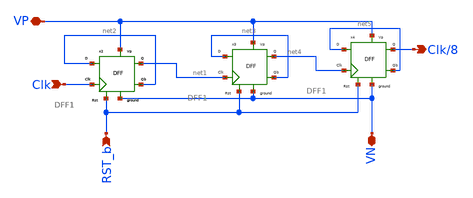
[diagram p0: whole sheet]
** sch_path: Blocks/Divide by 8 ckt/div8.sch
**.subckt div8 Clk Clk/8 RST_b VN VP
*.ipin Clk
*.opin Clk/8
*.ipin RST_b
*.iopin VN
*.iopin VP
x1 net2 Clk RST_b VN VP net1 net2 DFF1
x2 net2 Clk RST_b VN VP net1 net2 DFF1
x3 net3 net1 RST_b VN VP net4 net3 DFF1
x4 net5 net4 RST_b VN VP Clk/8 net5 DFF1
**.ends

* expanding   symbol:  PICO_2022/FlipFlops/DFF1.sym # of pins=7
** sym_path: component/FlipFlops/DFF1.sym
** sch_path: component/FlipFlops/DFF1.sch
.subckt DFF1 D Clk RST VN VP Q Qb
*.opin Q
*.iopin VN
*.iopin VP
*.ipin Clk
*.ipin D
*.ipin RST
*.opin Qb
x7 net2 net4 net3 VP VN NAND
x8 net3 Clk RST VP VN net2 NAND3
x6 Q net1 RST VP VN Qb NAND3
x4 net2 Clk net4 VP VN net1 NAND3
x5 net1 D RST VP VN net4 NAND3
x1 Qb net2 Q VP VN NAND
.ends


* expanding   symbol:  component/NAND2/NAND.sym # of pins=5
** sym_path: component/NAND2/NAND.sym
** sch_path: component/NAND2/NAND.sch
.subckt NAND B A Y VP VN
*.iopin VP
*.ipin A
*.ipin B
*.opin Y
*.iopin VN
XM1 Y A VP VP sky130_fd_pr__pfet_01v8 L=0.15 W=1.26 nf=1 ad='int((nf+1)/2) * W/nf * 0.29' as='int((nf+2)/2) * W/nf * 0.29'
+ pd='2*int((nf+1)/2) * (W/nf + 0.29)' ps='2*int((nf+2)/2) * (W/nf + 0.29)' nrd='0.29 / W' nrs='0.29 / W'
+ sa=0 sb=0 sd=0 mult=1 m=1
XM2 Y B VP VP sky130_fd_pr__pfet_01v8 L=0.15 W=1.26 nf=1 ad='int((nf+1)/2) * W/nf * 0.29' as='int((nf+2)/2) * W/nf * 0.29'
+ pd='2*int((nf+1)/2) * (W/nf + 0.29)' ps='2*int((nf+2)/2) * (W/nf + 0.29)' nrd='0.29 / W' nrs='0.29 / W'
+ sa=0 sb=0 sd=0 mult=1 m=1
XM3 Y A net1 net1 sky130_fd_pr__nfet_01v8 L=0.15 W=0.84 nf=1 ad='int((nf+1)/2) * W/nf * 0.29' as='int((nf+2)/2) * W/nf * 0.29'
+ pd='2*int((nf+1)/2) * (W/nf + 0.29)' ps='2*int((nf+2)/2) * (W/nf + 0.29)' nrd='0.29 / W' nrs='0.29 / W'
+ sa=0 sb=0 sd=0 mult=1 m=1
XM4 net1 B VN VN sky130_fd_pr__nfet_01v8 L=0.15 W=0.84 nf=1 ad='int((nf+1)/2) * W/nf * 0.29' as='int((nf+2)/2) * W/nf * 0.29'
+ pd='2*int((nf+1)/2) * (W/nf + 0.29)' ps='2*int((nf+2)/2) * (W/nf + 0.29)' nrd='0.29 / W' nrs='0.29 / W'
+ sa=0 sb=0 sd=0 mult=1 m=1
.ends


* expanding   symbol:  component/NAND3/NAND3.sym # of pins=6
** sym_path: component/NAND3/NAND3.sym
** sch_path: component/NAND3/NAND3.sch
.subckt NAND3 A B C VP VN Y
*.iopin VP
*.iopin VN
*.ipin A
*.ipin B
*.ipin C
*.opin Y
XM1 Y A net1 VN sky130_fd_pr__nfet_01v8 L=0.15 W=1.26 nf=1 ad='int((nf+1)/2) * W/nf * 0.29' as='int((nf+2)/2) * W/nf * 0.29'
+ pd='2*int((nf+1)/2) * (W/nf + 0.29)' ps='2*int((nf+2)/2) * (W/nf + 0.29)' nrd='0.29 / W' nrs='0.29 / W'
+ sa=0 sb=0 sd=0 mult=1 m=1
XM2 net1 B net2 VN sky130_fd_pr__nfet_01v8 L=0.15 W=1.26 nf=1 ad='int((nf+1)/2) * W/nf * 0.29' as='int((nf+2)/2) * W/nf * 0.29'
+ pd='2*int((nf+1)/2) * (W/nf + 0.29)' ps='2*int((nf+2)/2) * (W/nf + 0.29)' nrd='0.29 / W' nrs='0.29 / W'
+ sa=0 sb=0 sd=0 mult=1 m=1
XM3 net2 C VN VN sky130_fd_pr__nfet_01v8 L=0.15 W=1.26 nf=1 ad='int((nf+1)/2) * W/nf * 0.29' as='int((nf+2)/2) * W/nf * 0.29'
+ pd='2*int((nf+1)/2) * (W/nf + 0.29)' ps='2*int((nf+2)/2) * (W/nf + 0.29)' nrd='0.29 / W' nrs='0.29 / W'
+ sa=0 sb=0 sd=0 mult=1 m=1
XM4 Y A VP VP sky130_fd_pr__pfet_01v8 L=0.15 W=1.26 nf=1 ad='int((nf+1)/2) * W/nf * 0.29' as='int((nf+2)/2) * W/nf * 0.29'
+ pd='2*int((nf+1)/2) * (W/nf + 0.29)' ps='2*int((nf+2)/2) * (W/nf + 0.29)' nrd='0.29 / W' nrs='0.29 / W'
+ sa=0 sb=0 sd=0 mult=1 m=1
XM5 Y B VP VP sky130_fd_pr__pfet_01v8 L=0.15 W=1.26 nf=1 ad='int((nf+1)/2) * W/nf * 0.29' as='int((nf+2)/2) * W/nf * 0.29'
+ pd='2*int((nf+1)/2) * (W/nf + 0.29)' ps='2*int((nf+2)/2) * (W/nf + 0.29)' nrd='0.29 / W' nrs='0.29 / W'
+ sa=0 sb=0 sd=0 mult=1 m=1
XM6 Y C VP VP sky130_fd_pr__pfet_01v8 L=0.15 W=1.26 nf=1 ad='int((nf+1)/2) * W/nf * 0.29' as='int((nf+2)/2) * W/nf * 0.29'
+ pd='2*int((nf+1)/2) * (W/nf + 0.29)' ps='2*int((nf+2)/2) * (W/nf + 0.29)' nrd='0.29 / W' nrs='0.29 / W'
+ sa=0 sb=0 sd=0 mult=1 m=1
.ends

.end
